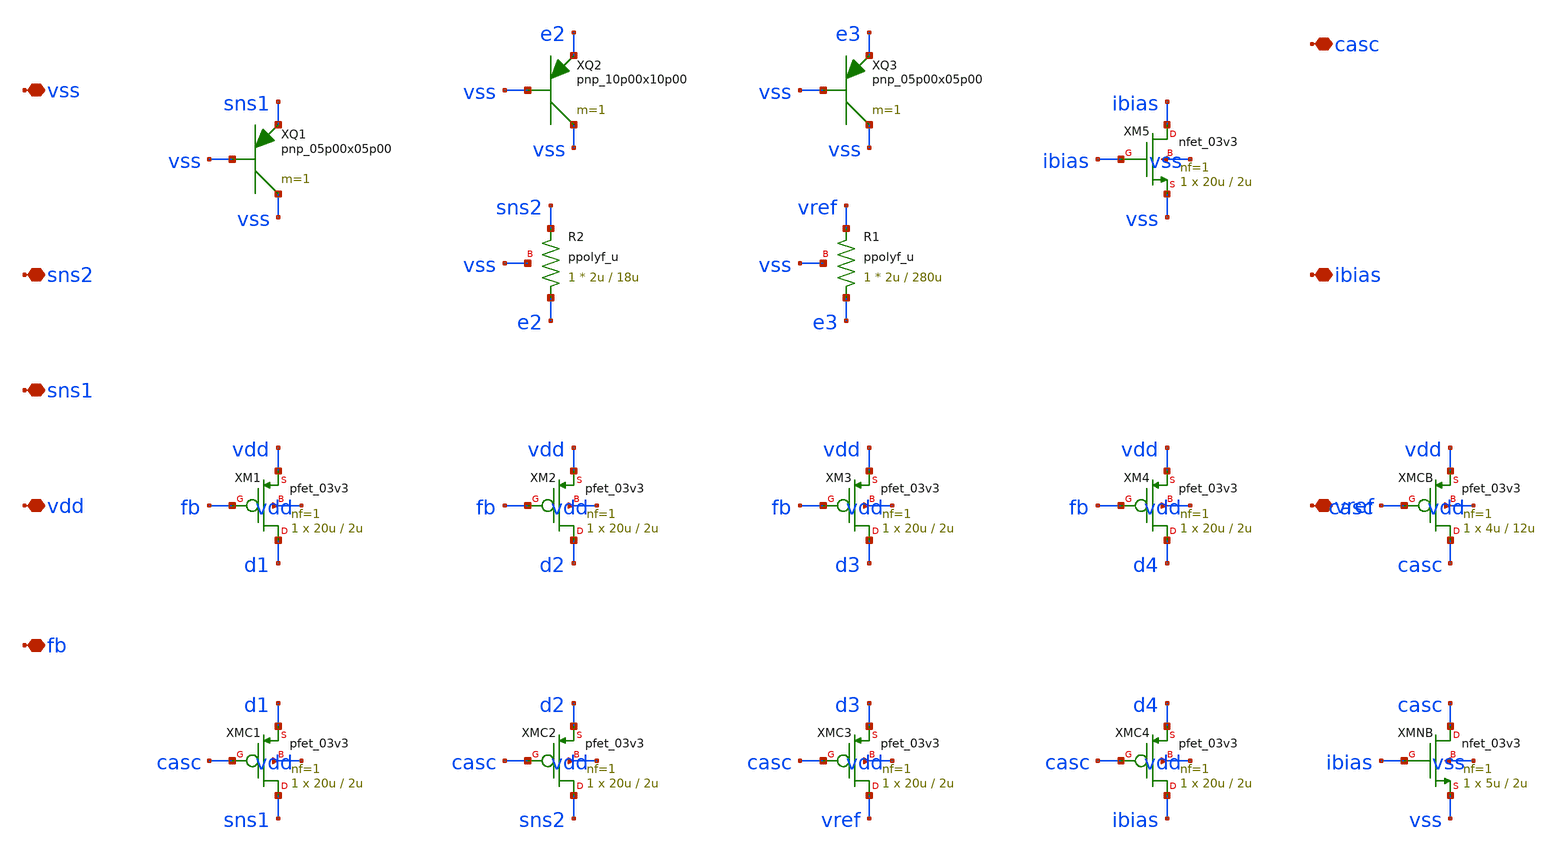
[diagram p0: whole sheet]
** sch_path: design/bandgap_core.sch
**.subckt bandgap_core vdd vss fb sns1 sns2 vref ibias casc
*.iopin vdd
*.iopin vss
*.iopin fb
*.iopin sns1
*.iopin sns2
*.iopin vref
*.iopin ibias
*.iopin casc
XM1 d1 fb vdd vdd pfet_03v3 L=2u W=20u nf=1 ad='int((nf+1)/2) * W/nf * 0.18u' as='int((nf+2)/2) * W/nf * 0.18u'
+ pd='2*int((nf+1)/2) * (W/nf + 0.18u)' ps='2*int((nf+2)/2) * (W/nf + 0.18u)' nrd='0.18u / W' nrs='0.18u / W'
+ sa=0 sb=0 sd=0 m=1
XMC1 sns1 casc d1 vdd pfet_03v3 L=2u W=20u nf=1 ad='int((nf+1)/2) * W/nf * 0.18u' as='int((nf+2)/2) * W/nf * 0.18u'
+ pd='2*int((nf+1)/2) * (W/nf + 0.18u)' ps='2*int((nf+2)/2) * (W/nf + 0.18u)' nrd='0.18u / W' nrs='0.18u / W'
+ sa=0 sb=0 sd=0 m=1
XQ1 vss vss sns1 pnp_05p00x05p00 m=1 par=1
XM2 d2 fb vdd vdd pfet_03v3 L=2u W=20u nf=1 ad='int((nf+1)/2) * W/nf * 0.18u' as='int((nf+2)/2) * W/nf * 0.18u'
+ pd='2*int((nf+1)/2) * (W/nf + 0.18u)' ps='2*int((nf+2)/2) * (W/nf + 0.18u)' nrd='0.18u / W' nrs='0.18u / W'
+ sa=0 sb=0 sd=0 m=1
XMC2 sns2 casc d2 vdd pfet_03v3 L=2u W=20u nf=1 ad='int((nf+1)/2) * W/nf * 0.18u' as='int((nf+2)/2) * W/nf * 0.18u'
+ pd='2*int((nf+1)/2) * (W/nf + 0.18u)' ps='2*int((nf+2)/2) * (W/nf + 0.18u)' nrd='0.18u / W' nrs='0.18u / W'
+ sa=0 sb=0 sd=0 m=1
XR2 e2 sns2 vss ppolyf_u r_width=2u r_length=18u m=1
XQ2 vss vss e2 pnp_10p00x10p00 m=1
XM3 d3 fb vdd vdd pfet_03v3 L=2u W=20u nf=1 ad='int((nf+1)/2) * W/nf * 0.18u' as='int((nf+2)/2) * W/nf * 0.18u'
+ pd='2*int((nf+1)/2) * (W/nf + 0.18u)' ps='2*int((nf+2)/2) * (W/nf + 0.18u)' nrd='0.18u / W' nrs='0.18u / W'
+ sa=0 sb=0 sd=0 m=1
XMC3 vref casc d3 vdd pfet_03v3 L=2u W=20u nf=1 ad='int((nf+1)/2) * W/nf * 0.18u' as='int((nf+2)/2) * W/nf * 0.18u'
+ pd='2*int((nf+1)/2) * (W/nf + 0.18u)' ps='2*int((nf+2)/2) * (W/nf + 0.18u)' nrd='0.18u / W' nrs='0.18u / W'
+ sa=0 sb=0 sd=0 m=1
XR1 e3 vref vss ppolyf_u r_width=2u r_length=280u m=1
XQ3 vss vss e3 pnp_05p00x05p00 m=1 par=1
XM4 d4 fb vdd vdd pfet_03v3 L=2u W=20u nf=1 ad='int((nf+1)/2) * W/nf * 0.18u' as='int((nf+2)/2) * W/nf * 0.18u'
+ pd='2*int((nf+1)/2) * (W/nf + 0.18u)' ps='2*int((nf+2)/2) * (W/nf + 0.18u)' nrd='0.18u / W' nrs='0.18u / W'
+ sa=0 sb=0 sd=0 m=1
XMC4 ibias casc d4 vdd pfet_03v3 L=2u W=20u nf=1 ad='int((nf+1)/2) * W/nf * 0.18u' as='int((nf+2)/2) * W/nf * 0.18u'
+ pd='2*int((nf+1)/2) * (W/nf + 0.18u)' ps='2*int((nf+2)/2) * (W/nf + 0.18u)' nrd='0.18u / W' nrs='0.18u / W'
+ sa=0 sb=0 sd=0 m=1
XM5 ibias ibias vss vss nfet_03v3 L=2u W=20u nf=1 ad='int((nf+1)/2) * W/nf * 0.18u' as='int((nf+2)/2) * W/nf * 0.18u'
+ pd='2*int((nf+1)/2) * (W/nf + 0.18u)' ps='2*int((nf+2)/2) * (W/nf + 0.18u)' nrd='0.18u / W' nrs='0.18u / W'
+ sa=0 sb=0 sd=0 m=1
XMCB casc casc vdd vdd pfet_03v3 L=12u W=4u nf=1 ad='int((nf+1)/2) * W/nf * 0.18u' as='int((nf+2)/2) * W/nf * 0.18u'
+ pd='2*int((nf+1)/2) * (W/nf + 0.18u)' ps='2*int((nf+2)/2) * (W/nf + 0.18u)' nrd='0.18u / W' nrs='0.18u / W'
+ sa=0 sb=0 sd=0 m=1
XMNB casc ibias vss vss nfet_03v3 L=2u W=5u nf=1 ad='int((nf+1)/2) * W/nf * 0.18u' as='int((nf+2)/2) * W/nf * 0.18u'
+ pd='2*int((nf+1)/2) * (W/nf + 0.18u)' ps='2*int((nf+2)/2) * (W/nf + 0.18u)' nrd='0.18u / W' nrs='0.18u / W'
+ sa=0 sb=0 sd=0 m=1
**.ends
.end
